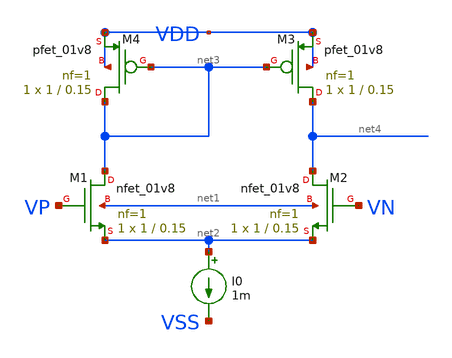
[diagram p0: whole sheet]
** sch_path: designs/libs/core_analog/p-ota/examples/fet-tb/diffpair2.sch
**.subckt diffpair2
XM1 net3 VP net2 net1 sky130_fd_pr__nfet_01v8 L=0.15 W=1 nf=1 ad='int((nf+1)/2) * W/nf * 0.29' as='int((nf+2)/2) * W/nf * 0.29'
+ pd='2*int((nf+1)/2) * (W/nf + 0.29)' ps='2*int((nf+2)/2) * (W/nf + 0.29)' nrd='0.29 / W' nrs='0.29 / W'
+ sa=0 sb=0 sd=0 mult=1 m=1
XM2 net4 VN net2 net1 sky130_fd_pr__nfet_01v8 L=0.15 W=1 nf=1 ad='int((nf+1)/2) * W/nf * 0.29' as='int((nf+2)/2) * W/nf * 0.29'
+ pd='2*int((nf+1)/2) * (W/nf + 0.29)' ps='2*int((nf+2)/2) * (W/nf + 0.29)' nrd='0.29 / W' nrs='0.29 / W'
+ sa=0 sb=0 sd=0 mult=1 m=1
XM3 net4 net3 VDD VDD sky130_fd_pr__pfet_01v8 L=0.15 W=1 nf=1 ad='int((nf+1)/2) * W/nf * 0.29' as='int((nf+2)/2) * W/nf * 0.29'
+ pd='2*int((nf+1)/2) * (W/nf + 0.29)' ps='2*int((nf+2)/2) * (W/nf + 0.29)' nrd='0.29 / W' nrs='0.29 / W'
+ sa=0 sb=0 sd=0 mult=1 m=1
XM4 net3 net3 VDD VDD sky130_fd_pr__pfet_01v8 L=0.15 W=1 nf=1 ad='int((nf+1)/2) * W/nf * 0.29' as='int((nf+2)/2) * W/nf * 0.29'
+ pd='2*int((nf+1)/2) * (W/nf + 0.29)' ps='2*int((nf+2)/2) * (W/nf + 0.29)' nrd='0.29 / W' nrs='0.29 / W'
+ sa=0 sb=0 sd=0 mult=1 m=1
I0 net2 VSS 1m
**.ends
.end
